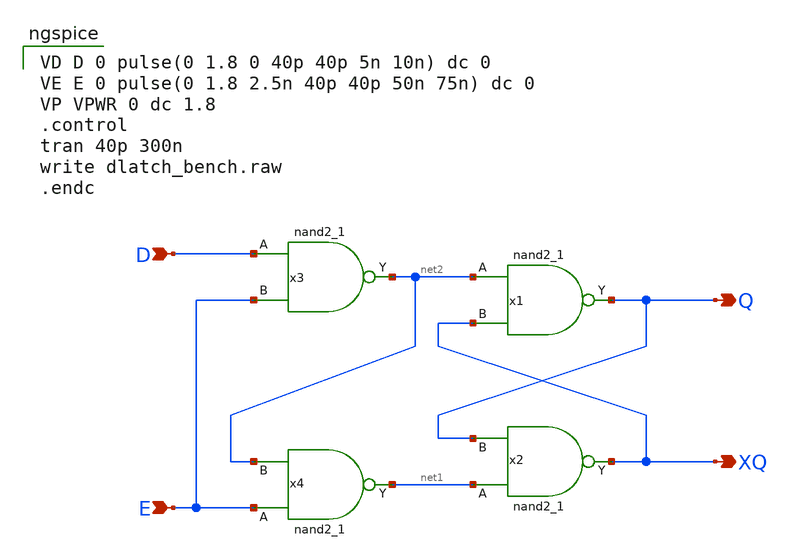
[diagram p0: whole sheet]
** sch_path: dlatch_bench.sch
**.subckt dlatch_bench E D Q XQ
*.ipin E
*.ipin D
*.opin Q
*.opin XQ
x1 net2 XQ 0 0 VPWR VPWR Q sky130_fd_sc_hd__nand2_1
x2 net1 Q 0 0 VPWR VPWR XQ sky130_fd_sc_hd__nand2_1
x3 D E 0 0 VPWR VPWR net2 sky130_fd_sc_hd__nand2_1
x4 E net2 0 0 VPWR VPWR net1 sky130_fd_sc_hd__nand2_1
**** begin user architecture code

VD D 0 pulse(0 1.8 0 40p 40p 5n 10n) dc 0
VE E 0 pulse(0 1.8 2.5n 40p 40p 50n 75n) dc 0
VP VPWR 0 dc 1.8
.control
tran 40p 300n
write dlatch_bench.raw
.endc


** opencircuitdesign pdks install
.lib $::SKYWATER_MODELS/sky130.lib.spice tt
.include $::SKYWATER_STDCELLS/sky130_fd_sc_hd.spice

**** end user architecture code
**.ends
.end
